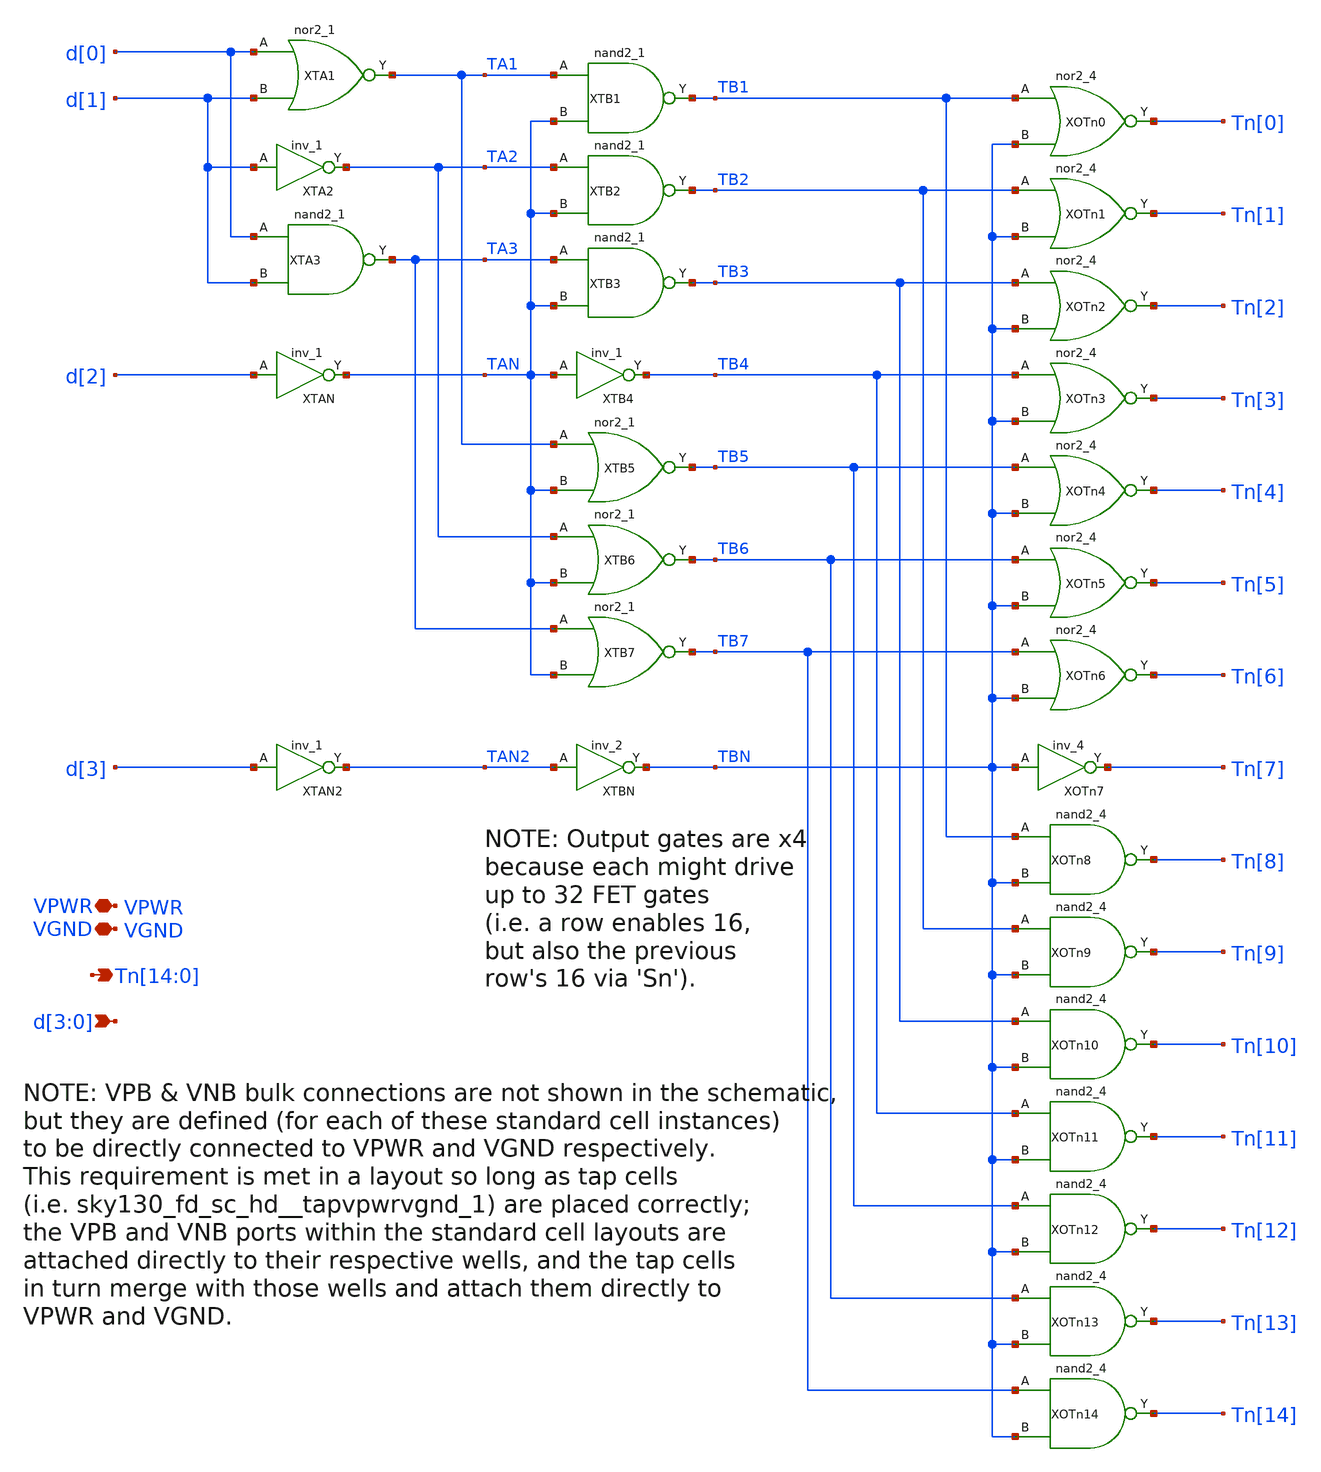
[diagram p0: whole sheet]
** sch_path: xschem/thermo15.sch
**.subckt thermo15 VPWR d[3],d[2],d[1],d[0] VGND
*+ Tn[14],Tn[13],Tn[12],Tn[11],Tn[10],Tn[9],Tn[8],Tn[7],Tn[6],Tn[5],Tn[4],Tn[3],Tn[2],Tn[1],Tn[0]
*.iopin VPWR
*.ipin d[3],d[2],d[1],d[0]
*.iopin VGND
*.opin
*+ Tn[14],Tn[13],Tn[12],Tn[11],Tn[10],Tn[9],Tn[8],Tn[7],Tn[6],Tn[5],Tn[4],Tn[3],Tn[2],Tn[1],Tn[0]
XTA2 d[1] VGND VGND VPWR VPWR TA2 sky130_fd_sc_hd__inv_1
XTBN TAN2 VGND VGND VPWR VPWR TBN sky130_fd_sc_hd__inv_2
XTA3 d[0] d[1] VGND VGND VPWR VPWR TA3 sky130_fd_sc_hd__nand2_1
XTA1 d[0] d[1] VGND VGND VPWR VPWR TA1 sky130_fd_sc_hd__nor2_1
XTAN d[2] VGND VGND VPWR VPWR TAN sky130_fd_sc_hd__inv_1
XTB1 TA1 TAN VGND VGND VPWR VPWR TB1 sky130_fd_sc_hd__nand2_1
XTB2 TA2 TAN VGND VGND VPWR VPWR TB2 sky130_fd_sc_hd__nand2_1
XTB3 TA3 TAN VGND VGND VPWR VPWR TB3 sky130_fd_sc_hd__nand2_1
XTB4 TAN VGND VGND VPWR VPWR TB4 sky130_fd_sc_hd__inv_1
XTB5 TA1 TAN VGND VGND VPWR VPWR TB5 sky130_fd_sc_hd__nor2_1
XTB6 TA2 TAN VGND VGND VPWR VPWR TB6 sky130_fd_sc_hd__nor2_1
XTB7 TA3 TAN VGND VGND VPWR VPWR TB7 sky130_fd_sc_hd__nor2_1
XOTn0 TB1 TBN VGND VGND VPWR VPWR Tn[0] sky130_fd_sc_hd__nor2_4
XOTn1 TB2 TBN VGND VGND VPWR VPWR Tn[1] sky130_fd_sc_hd__nor2_4
XOTn2 TB3 TBN VGND VGND VPWR VPWR Tn[2] sky130_fd_sc_hd__nor2_4
XOTn3 TB4 TBN VGND VGND VPWR VPWR Tn[3] sky130_fd_sc_hd__nor2_4
XOTn4 TB5 TBN VGND VGND VPWR VPWR Tn[4] sky130_fd_sc_hd__nor2_4
XOTn5 TB6 TBN VGND VGND VPWR VPWR Tn[5] sky130_fd_sc_hd__nor2_4
XOTn6 TB7 TBN VGND VGND VPWR VPWR Tn[6] sky130_fd_sc_hd__nor2_4
XOTn7 TBN VGND VGND VPWR VPWR Tn[7] sky130_fd_sc_hd__inv_4
XOTn8 TB1 TBN VGND VGND VPWR VPWR Tn[8] sky130_fd_sc_hd__nand2_4
XOTn9 TB2 TBN VGND VGND VPWR VPWR Tn[9] sky130_fd_sc_hd__nand2_4
XOTn10 TB3 TBN VGND VGND VPWR VPWR Tn[10] sky130_fd_sc_hd__nand2_4
XOTn11 TB4 TBN VGND VGND VPWR VPWR Tn[11] sky130_fd_sc_hd__nand2_4
XOTn12 TB5 TBN VGND VGND VPWR VPWR Tn[12] sky130_fd_sc_hd__nand2_4
XOTn13 TB6 TBN VGND VGND VPWR VPWR Tn[13] sky130_fd_sc_hd__nand2_4
XOTn14 TB7 TBN VGND VGND VPWR VPWR Tn[14] sky130_fd_sc_hd__nand2_4
XTAN2 d[3] VGND VGND VPWR VPWR TAN2 sky130_fd_sc_hd__inv_1
**.ends
.end
